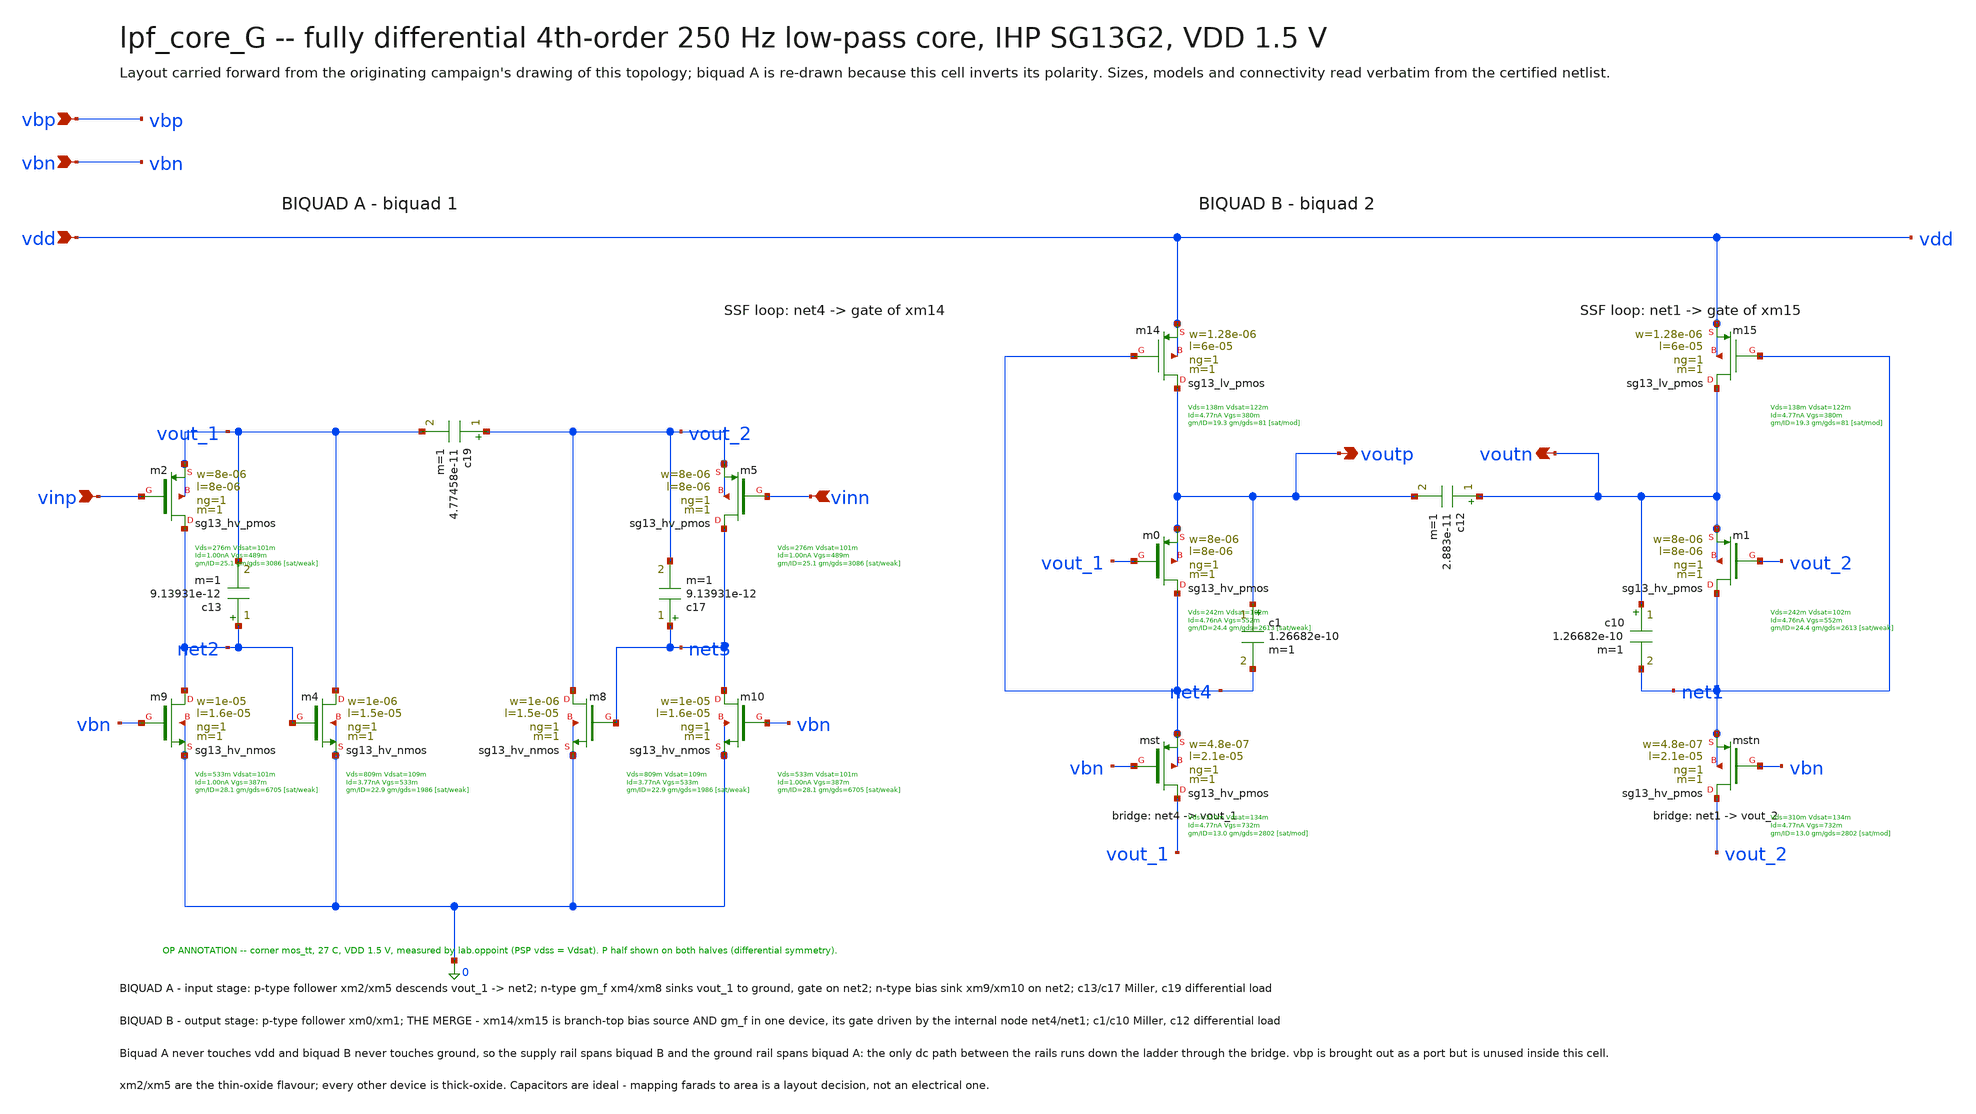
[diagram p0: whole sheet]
** sch_path: signoff/G-maxthd/lpf_core_G.sch
**.subckt lpf_core_G vinp vinn voutp voutn vdd vbn vbp
*.ipin vinp
*.ipin vinn
*.opin voutp
*.opin voutn
*.ipin vdd
*.ipin vbn
*.ipin vbp
Xm2 net2 vinp vout_1 vout_1 sg13_hv_pmos w=8e-06 l=8e-06 ng=1 m=1 mm_ok=1
Xm5 net3 vinn vout_2 vout_2 sg13_hv_pmos w=8e-06 l=8e-06 ng=1 m=1 mm_ok=1
Xm4 vout_1 net2 0 0 sg13_hv_nmos w=1e-06 l=1.5e-05 ng=1 m=1 mm_ok=1
Xm8 vout_2 net3 0 0 sg13_hv_nmos w=1e-06 l=1.5e-05 ng=1 m=1 mm_ok=1
Xm9 net2 vbn 0 0 sg13_hv_nmos w=1e-05 l=1.6e-05 ng=1 m=1 mm_ok=1
Xm10 net3 vbn 0 0 sg13_hv_nmos w=1e-05 l=1.6e-05 ng=1 m=1 mm_ok=1
Xmst vout_1 vbn net4 net4 sg13_hv_pmos w=4.8e-07 l=2.1e-05 ng=1 m=1 mm_ok=1
Xmstn vout_2 vbn net1 net1 sg13_hv_pmos w=4.8e-07 l=2.1e-05 ng=1 m=1 mm_ok=1
Xm0 net4 vout_1 voutp voutp sg13_hv_pmos w=8e-06 l=8e-06 ng=1 m=1 mm_ok=1
Xm1 net1 vout_2 voutn voutn sg13_hv_pmos w=8e-06 l=8e-06 ng=1 m=1 mm_ok=1
Xm14 voutp net4 vdd vdd sg13_lv_pmos w=1.28e-06 l=6e-05 ng=1 m=1 mm_ok=1
Xm15 voutn net1 vdd vdd sg13_lv_pmos w=1.28e-06 l=6e-05 ng=1 m=1 mm_ok=1
c13 net2 vout_1 9.13931e-12 m=1
c17 net3 vout_2 9.13931e-12 m=1
c19 vout_2 vout_1 4.77458e-11 m=1
c1 voutp net4 1.26682e-10 m=1
c10 voutn net1 1.26682e-10 m=1
c12 voutn voutp 2.883e-11 m=1
**.ends
.end
